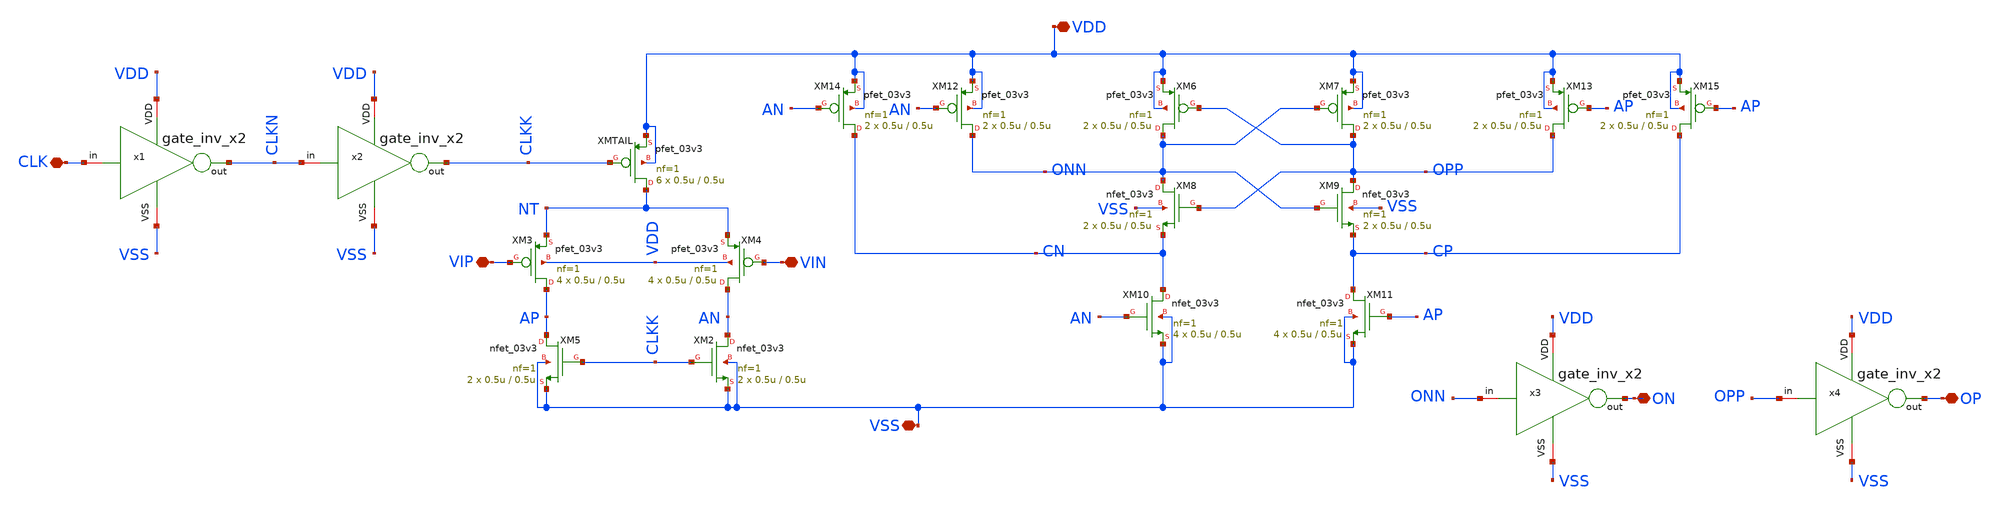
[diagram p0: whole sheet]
** sch_path: designs/sar_adc/comparator/StrongARM/xschem/strongARM.sch
**.subckt strongARM VSS VDD VIN VIP OP CLK ON
*.iopin VSS
*.iopin VDD
*.iopin VIN
*.iopin VIP
*.iopin OP
*.iopin CLK
*.iopin ON
XMTAIL NT CLKK VDD VDD pfet_03v3 L=0.5u W=0.5u nf=1 ad='int((nf+1)/2) * W/nf * 0.18u' as='int((nf+2)/2) * W/nf * 0.18u'
+ pd='2*int((nf+1)/2) * (W/nf + 0.18u)' ps='2*int((nf+2)/2) * (W/nf + 0.18u)' nrd='0.18u / W' nrs='0.18u / W'
+ sa=0 sb=0 sd=0 m=6
XM2 AN CLKK VSS VSS nfet_03v3 L=0.5u W=0.5u nf=1 ad='int((nf+1)/2) * W/nf * 0.18u' as='int((nf+2)/2) * W/nf * 0.18u'
+ pd='2*int((nf+1)/2) * (W/nf + 0.18u)' ps='2*int((nf+2)/2) * (W/nf + 0.18u)' nrd='0.18u / W' nrs='0.18u / W'
+ sa=0 sb=0 sd=0 m=2
XM3 AP VIP NT VDD pfet_03v3 L=0.5u W=0.5u nf=1 ad='int((nf+1)/2) * W/nf * 0.18u' as='int((nf+2)/2) * W/nf * 0.18u'
+ pd='2*int((nf+1)/2) * (W/nf + 0.18u)' ps='2*int((nf+2)/2) * (W/nf + 0.18u)' nrd='0.18u / W' nrs='0.18u / W'
+ sa=0 sb=0 sd=0 m=4
XM4 AN VIN NT VDD pfet_03v3 L=0.5u W=0.5u nf=1 ad='int((nf+1)/2) * W/nf * 0.18u' as='int((nf+2)/2) * W/nf * 0.18u'
+ pd='2*int((nf+1)/2) * (W/nf + 0.18u)' ps='2*int((nf+2)/2) * (W/nf + 0.18u)' nrd='0.18u / W' nrs='0.18u / W'
+ sa=0 sb=0 sd=0 m=4
XM5 AP CLKK VSS VSS nfet_03v3 L=0.5u W=0.5u nf=1 ad='int((nf+1)/2) * W/nf * 0.18u' as='int((nf+2)/2) * W/nf * 0.18u'
+ pd='2*int((nf+1)/2) * (W/nf + 0.18u)' ps='2*int((nf+2)/2) * (W/nf + 0.18u)' nrd='0.18u / W' nrs='0.18u / W'
+ sa=0 sb=0 sd=0 m=2
XM6 ONN OPP VDD VDD pfet_03v3 L=0.5u W=0.5u nf=1 ad='int((nf+1)/2) * W/nf * 0.18u' as='int((nf+2)/2) * W/nf * 0.18u'
+ pd='2*int((nf+1)/2) * (W/nf + 0.18u)' ps='2*int((nf+2)/2) * (W/nf + 0.18u)' nrd='0.18u / W' nrs='0.18u / W'
+ sa=0 sb=0 sd=0 m=2
XM7 OPP ONN VDD VDD pfet_03v3 L=0.5u W=0.5u nf=1 ad='int((nf+1)/2) * W/nf * 0.18u' as='int((nf+2)/2) * W/nf * 0.18u'
+ pd='2*int((nf+1)/2) * (W/nf + 0.18u)' ps='2*int((nf+2)/2) * (W/nf + 0.18u)' nrd='0.18u / W' nrs='0.18u / W'
+ sa=0 sb=0 sd=0 m=2
XM8 ONN OPP CN VSS nfet_03v3 L=0.5u W=0.5u nf=1 ad='int((nf+1)/2) * W/nf * 0.18u' as='int((nf+2)/2) * W/nf * 0.18u'
+ pd='2*int((nf+1)/2) * (W/nf + 0.18u)' ps='2*int((nf+2)/2) * (W/nf + 0.18u)' nrd='0.18u / W' nrs='0.18u / W'
+ sa=0 sb=0 sd=0 m=2
XM9 OPP ONN CP VSS nfet_03v3 L=0.5u W=0.5u nf=1 ad='int((nf+1)/2) * W/nf * 0.18u' as='int((nf+2)/2) * W/nf * 0.18u'
+ pd='2*int((nf+1)/2) * (W/nf + 0.18u)' ps='2*int((nf+2)/2) * (W/nf + 0.18u)' nrd='0.18u / W' nrs='0.18u / W'
+ sa=0 sb=0 sd=0 m=2
XM10 CN AN VSS VSS nfet_03v3 L=0.5u W=0.5u nf=1 ad='int((nf+1)/2) * W/nf * 0.18u' as='int((nf+2)/2) * W/nf * 0.18u'
+ pd='2*int((nf+1)/2) * (W/nf + 0.18u)' ps='2*int((nf+2)/2) * (W/nf + 0.18u)' nrd='0.18u / W' nrs='0.18u / W'
+ sa=0 sb=0 sd=0 m=4
XM11 CP AP VSS VSS nfet_03v3 L=0.5u W=0.5u nf=1 ad='int((nf+1)/2) * W/nf * 0.18u' as='int((nf+2)/2) * W/nf * 0.18u'
+ pd='2*int((nf+1)/2) * (W/nf + 0.18u)' ps='2*int((nf+2)/2) * (W/nf + 0.18u)' nrd='0.18u / W' nrs='0.18u / W'
+ sa=0 sb=0 sd=0 m=4
XM12 ONN AN VDD VDD pfet_03v3 L=0.5u W=0.5u nf=1 ad='int((nf+1)/2) * W/nf * 0.18u' as='int((nf+2)/2) * W/nf * 0.18u'
+ pd='2*int((nf+1)/2) * (W/nf + 0.18u)' ps='2*int((nf+2)/2) * (W/nf + 0.18u)' nrd='0.18u / W' nrs='0.18u / W'
+ sa=0 sb=0 sd=0 m=2
XM13 OPP AP VDD VDD pfet_03v3 L=0.5u W=0.5u nf=1 ad='int((nf+1)/2) * W/nf * 0.18u' as='int((nf+2)/2) * W/nf * 0.18u'
+ pd='2*int((nf+1)/2) * (W/nf + 0.18u)' ps='2*int((nf+2)/2) * (W/nf + 0.18u)' nrd='0.18u / W' nrs='0.18u / W'
+ sa=0 sb=0 sd=0 m=2
XM14 CN AN VDD VDD pfet_03v3 L=0.5u W=0.5u nf=1 ad='int((nf+1)/2) * W/nf * 0.18u' as='int((nf+2)/2) * W/nf * 0.18u'
+ pd='2*int((nf+1)/2) * (W/nf + 0.18u)' ps='2*int((nf+2)/2) * (W/nf + 0.18u)' nrd='0.18u / W' nrs='0.18u / W'
+ sa=0 sb=0 sd=0 m=2
XM15 CP AP VDD VDD pfet_03v3 L=0.5u W=0.5u nf=1 ad='int((nf+1)/2) * W/nf * 0.18u' as='int((nf+2)/2) * W/nf * 0.18u'
+ pd='2*int((nf+1)/2) * (W/nf + 0.18u)' ps='2*int((nf+2)/2) * (W/nf + 0.18u)' nrd='0.18u / W' nrs='0.18u / W'
+ sa=0 sb=0 sd=0 m=2
x1 VDD CLK CLKN VSS gate_inv_x2
x2 VDD CLKN CLKK VSS gate_inv_x2
x3 VDD ONN ON VSS gate_inv_x2
x4 VDD OPP OP VSS gate_inv_x2
**.ends

* expanding   symbol:  designs/sar_adc/digital/gate_inv_x2/xschem/gate_inv_x2.sym # of pins=6
** sym_path: designs/sar_adc/digital/gate_inv_x2/xschem/gate_inv_x2.sym
** sch_path: designs/sar_adc/digital/gate_inv_x2/xschem/gate_inv_x2.sch
.subckt gate_inv_x2 VDD in out VSS
*.opin out
*.iopin in
*.iopin VDD
*.iopin VSS
XM1 out in VSS VSS nfet_03v3 L=0.28u W=0.5u nf=1 ad='int((nf+1)/2) * W/nf * 0.18u' as='int((nf+2)/2) * W/nf * 0.18u'
+ pd='2*int((nf+1)/2) * (W/nf + 0.18u)' ps='2*int((nf+2)/2) * (W/nf + 0.18u)' nrd='0.18u / W' nrs='0.18u / W'
+ sa=0 sb=0 sd=0 m=2
XM2 out in VDD VDD pfet_03v3 L=0.28u W=0.5u nf=1 ad='int((nf+1)/2) * W/nf * 0.18u' as='int((nf+2)/2) * W/nf * 0.18u'
+ pd='2*int((nf+1)/2) * (W/nf + 0.18u)' ps='2*int((nf+2)/2) * (W/nf + 0.18u)' nrd='0.18u / W' nrs='0.18u / W'
+ sa=0 sb=0 sd=0 m=2
.ends

.end
